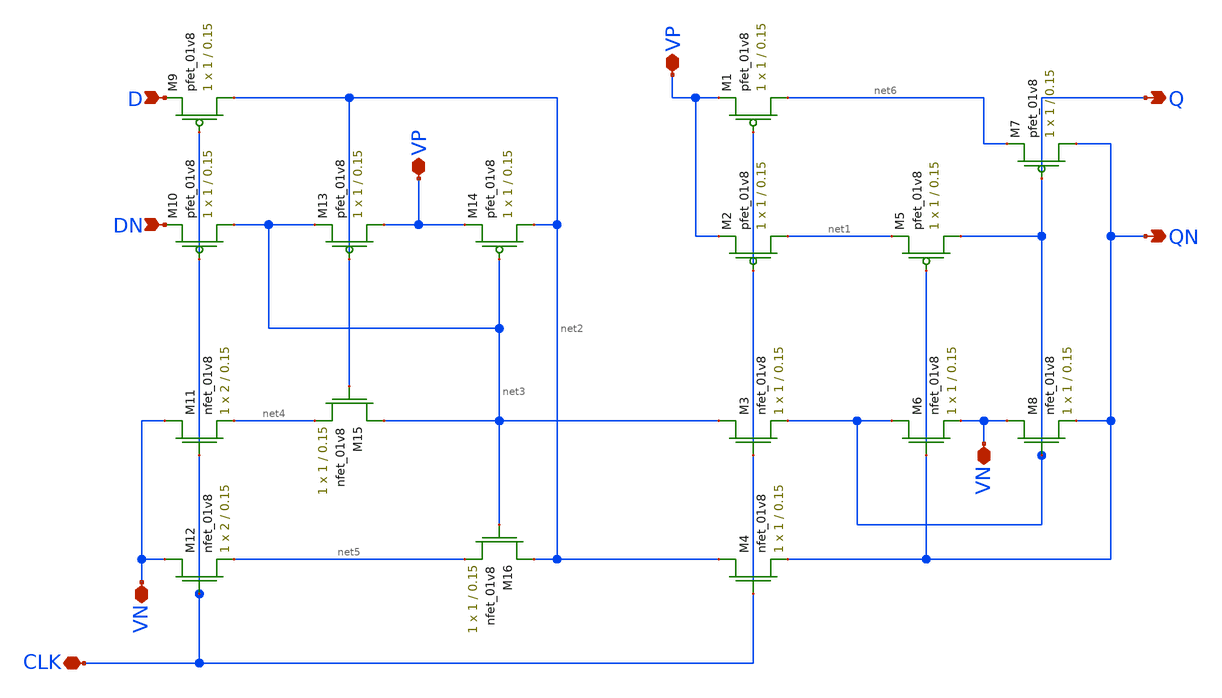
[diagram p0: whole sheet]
** sch_path: schematic/CSRL.sch
**.subckt CSRL CLK VP VP VN VN D DN QN Q
*.iopin CLK
*.iopin VP
*.iopin VP
*.iopin VN
*.iopin VN
*.ipin D
*.ipin DN
*.opin QN
*.opin Q
XM1 net6 CLK VP VDD sky130_fd_pr__pfet_01v8 L=0.15 W=1 nf=1 ad='int((nf+1)/2) * W/nf * 0.29' as='int((nf+2)/2) * W/nf * 0.29'
+ pd='2*int((nf+1)/2) * (W/nf + 0.29)' ps='2*int((nf+2)/2) * (W/nf + 0.29)' nrd='0.29 / W' nrs='0.29 / W'
+ sa=0 sb=0 sd=0 mult=1 m=1
XM2 net1 CLK VP VDD sky130_fd_pr__pfet_01v8 L=0.15 W=1 nf=1 ad='int((nf+1)/2) * W/nf * 0.29' as='int((nf+2)/2) * W/nf * 0.29'
+ pd='2*int((nf+1)/2) * (W/nf + 0.29)' ps='2*int((nf+2)/2) * (W/nf + 0.29)' nrd='0.29 / W' nrs='0.29 / W'
+ sa=0 sb=0 sd=0 mult=1 m=1
XM3 net3 CLK Q GND sky130_fd_pr__nfet_01v8 L=0.15 W=1 nf=1 ad='int((nf+1)/2) * W/nf * 0.29' as='int((nf+2)/2) * W/nf * 0.29'
+ pd='2*int((nf+1)/2) * (W/nf + 0.29)' ps='2*int((nf+2)/2) * (W/nf + 0.29)' nrd='0.29 / W' nrs='0.29 / W'
+ sa=0 sb=0 sd=0 mult=1 m=1
XM4 net2 CLK QN GND sky130_fd_pr__nfet_01v8 L=0.15 W=1 nf=1 ad='int((nf+1)/2) * W/nf * 0.29' as='int((nf+2)/2) * W/nf * 0.29'
+ pd='2*int((nf+1)/2) * (W/nf + 0.29)' ps='2*int((nf+2)/2) * (W/nf + 0.29)' nrd='0.29 / W' nrs='0.29 / W'
+ sa=0 sb=0 sd=0 mult=1 m=1
XM5 Q QN net1 VDD sky130_fd_pr__pfet_01v8 L=0.15 W=1 nf=1 ad='int((nf+1)/2) * W/nf * 0.29' as='int((nf+2)/2) * W/nf * 0.29'
+ pd='2*int((nf+1)/2) * (W/nf + 0.29)' ps='2*int((nf+2)/2) * (W/nf + 0.29)' nrd='0.29 / W' nrs='0.29 / W'
+ sa=0 sb=0 sd=0 mult=1 m=1
XM6 Q QN VN GND sky130_fd_pr__nfet_01v8 L=0.15 W=1 nf=1 ad='int((nf+1)/2) * W/nf * 0.29' as='int((nf+2)/2) * W/nf * 0.29'
+ pd='2*int((nf+1)/2) * (W/nf + 0.29)' ps='2*int((nf+2)/2) * (W/nf + 0.29)' nrd='0.29 / W' nrs='0.29 / W'
+ sa=0 sb=0 sd=0 mult=1 m=1
XM7 QN Q net6 VDD sky130_fd_pr__pfet_01v8 L=0.15 W=1 nf=1 ad='int((nf+1)/2) * W/nf * 0.29' as='int((nf+2)/2) * W/nf * 0.29'
+ pd='2*int((nf+1)/2) * (W/nf + 0.29)' ps='2*int((nf+2)/2) * (W/nf + 0.29)' nrd='0.29 / W' nrs='0.29 / W'
+ sa=0 sb=0 sd=0 mult=1 m=1
XM8 VN Q QN GND sky130_fd_pr__nfet_01v8 L=0.15 W=1 nf=1 ad='int((nf+1)/2) * W/nf * 0.29' as='int((nf+2)/2) * W/nf * 0.29'
+ pd='2*int((nf+1)/2) * (W/nf + 0.29)' ps='2*int((nf+2)/2) * (W/nf + 0.29)' nrd='0.29 / W' nrs='0.29 / W'
+ sa=0 sb=0 sd=0 mult=1 m=1
XM9 net2 CLK D VDD sky130_fd_pr__pfet_01v8 L=0.15 W=1 nf=1 ad='int((nf+1)/2) * W/nf * 0.29' as='int((nf+2)/2) * W/nf * 0.29'
+ pd='2*int((nf+1)/2) * (W/nf + 0.29)' ps='2*int((nf+2)/2) * (W/nf + 0.29)' nrd='0.29 / W' nrs='0.29 / W'
+ sa=0 sb=0 sd=0 mult=1 m=1
XM10 net3 CLK DN VDD sky130_fd_pr__pfet_01v8 L=0.15 W=1 nf=1 ad='int((nf+1)/2) * W/nf * 0.29' as='int((nf+2)/2) * W/nf * 0.29'
+ pd='2*int((nf+1)/2) * (W/nf + 0.29)' ps='2*int((nf+2)/2) * (W/nf + 0.29)' nrd='0.29 / W' nrs='0.29 / W'
+ sa=0 sb=0 sd=0 mult=1 m=1
XM11 VN CLK net4 GND sky130_fd_pr__nfet_01v8 L=0.15 W=2 nf=1 ad='int((nf+1)/2) * W/nf * 0.29' as='int((nf+2)/2) * W/nf * 0.29'
+ pd='2*int((nf+1)/2) * (W/nf + 0.29)' ps='2*int((nf+2)/2) * (W/nf + 0.29)' nrd='0.29 / W' nrs='0.29 / W'
+ sa=0 sb=0 sd=0 mult=1 m=1
XM12 VN CLK net5 GND sky130_fd_pr__nfet_01v8 L=0.15 W=2 nf=1 ad='int((nf+1)/2) * W/nf * 0.29' as='int((nf+2)/2) * W/nf * 0.29'
+ pd='2*int((nf+1)/2) * (W/nf + 0.29)' ps='2*int((nf+2)/2) * (W/nf + 0.29)' nrd='0.29 / W' nrs='0.29 / W'
+ sa=0 sb=0 sd=0 mult=1 m=1
XM13 VP net2 net3 VDD sky130_fd_pr__pfet_01v8 L=0.15 W=1 nf=1 ad='int((nf+1)/2) * W/nf * 0.29' as='int((nf+2)/2) * W/nf * 0.29'
+ pd='2*int((nf+1)/2) * (W/nf + 0.29)' ps='2*int((nf+2)/2) * (W/nf + 0.29)' nrd='0.29 / W' nrs='0.29 / W'
+ sa=0 sb=0 sd=0 mult=1 m=1
XM14 net2 net3 VP VDD sky130_fd_pr__pfet_01v8 L=0.15 W=1 nf=1 ad='int((nf+1)/2) * W/nf * 0.29' as='int((nf+2)/2) * W/nf * 0.29'
+ pd='2*int((nf+1)/2) * (W/nf + 0.29)' ps='2*int((nf+2)/2) * (W/nf + 0.29)' nrd='0.29 / W' nrs='0.29 / W'
+ sa=0 sb=0 sd=0 mult=1 m=1
XM15 net3 net2 net4 GND sky130_fd_pr__nfet_01v8 L=0.15 W=1 nf=1 ad='int((nf+1)/2) * W/nf * 0.29' as='int((nf+2)/2) * W/nf * 0.29'
+ pd='2*int((nf+1)/2) * (W/nf + 0.29)' ps='2*int((nf+2)/2) * (W/nf + 0.29)' nrd='0.29 / W' nrs='0.29 / W'
+ sa=0 sb=0 sd=0 mult=1 m=1
XM16 net2 net3 net5 GND sky130_fd_pr__nfet_01v8 L=0.15 W=1 nf=1 ad='int((nf+1)/2) * W/nf * 0.29' as='int((nf+2)/2) * W/nf * 0.29'
+ pd='2*int((nf+1)/2) * (W/nf + 0.29)' ps='2*int((nf+2)/2) * (W/nf + 0.29)' nrd='0.29 / W' nrs='0.29 / W'
+ sa=0 sb=0 sd=0 mult=1 m=1
**.ends
.end
